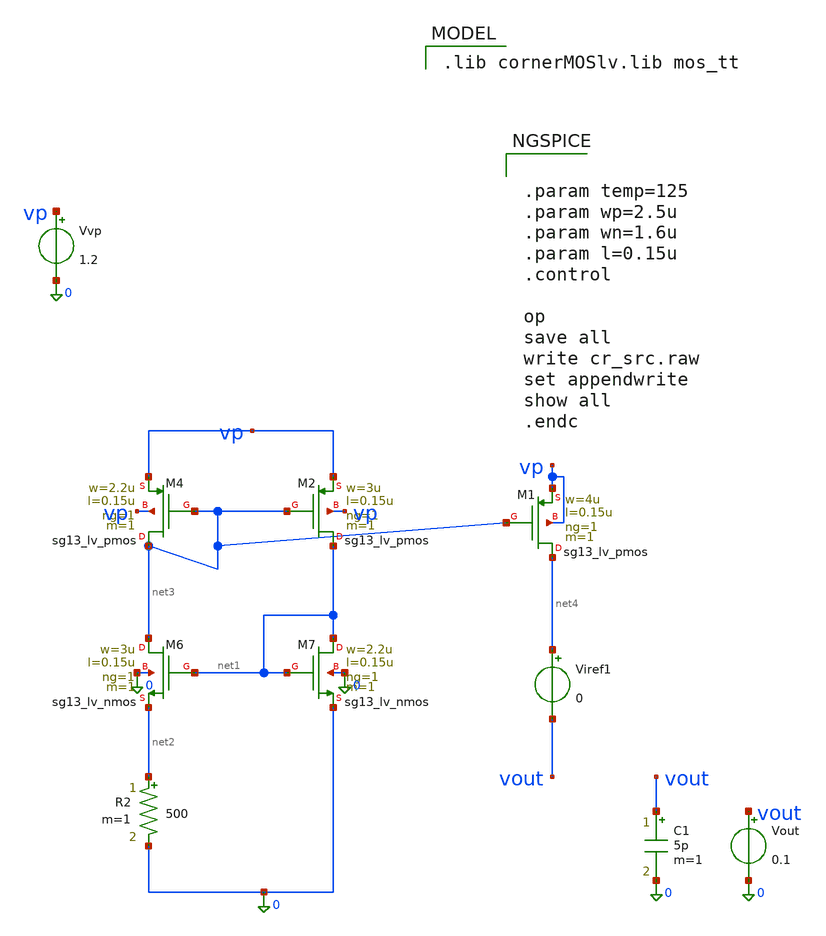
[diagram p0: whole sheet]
** sch_path: charge_pump/curr_source_tb.sch
**.subckt curr_source_tb
XM4 net3 net3 vp vp sg13_lv_pmos w=2.2u l=0.15u ng=1 m=1 mm_ok=1
XM2 net1 net3 vp vp sg13_lv_pmos w=3u l=0.15u ng=1 m=1 mm_ok=1
XM6 net3 net1 net2 0 sg13_lv_nmos w=3u l=0.15u ng=1 m=1 mm_ok=1
XM7 net1 net1 0 0 sg13_lv_nmos w=2.2u l=0.15u ng=1 m=1 mm_ok=1
R2 net2 0 500 m=1
Vvp vp 0 1.2
Viref1 net4 vout 0
XM1 net4 net3 vp vp sg13_lv_pmos w=4u l=0.15u ng=1 m=1 mm_ok=1
C1 vout 0 5p m=1
Vout vout 0 0.1
**** begin user architecture code
 .lib cornerMOSlv.lib mos_tt



.param temp=125
.param wp=2.5u
.param wn=1.6u
.param l=0.15u
.control

op
save all
write cr_src.raw
set appendwrite
show all
.endc


**** end user architecture code
**.ends
.end
